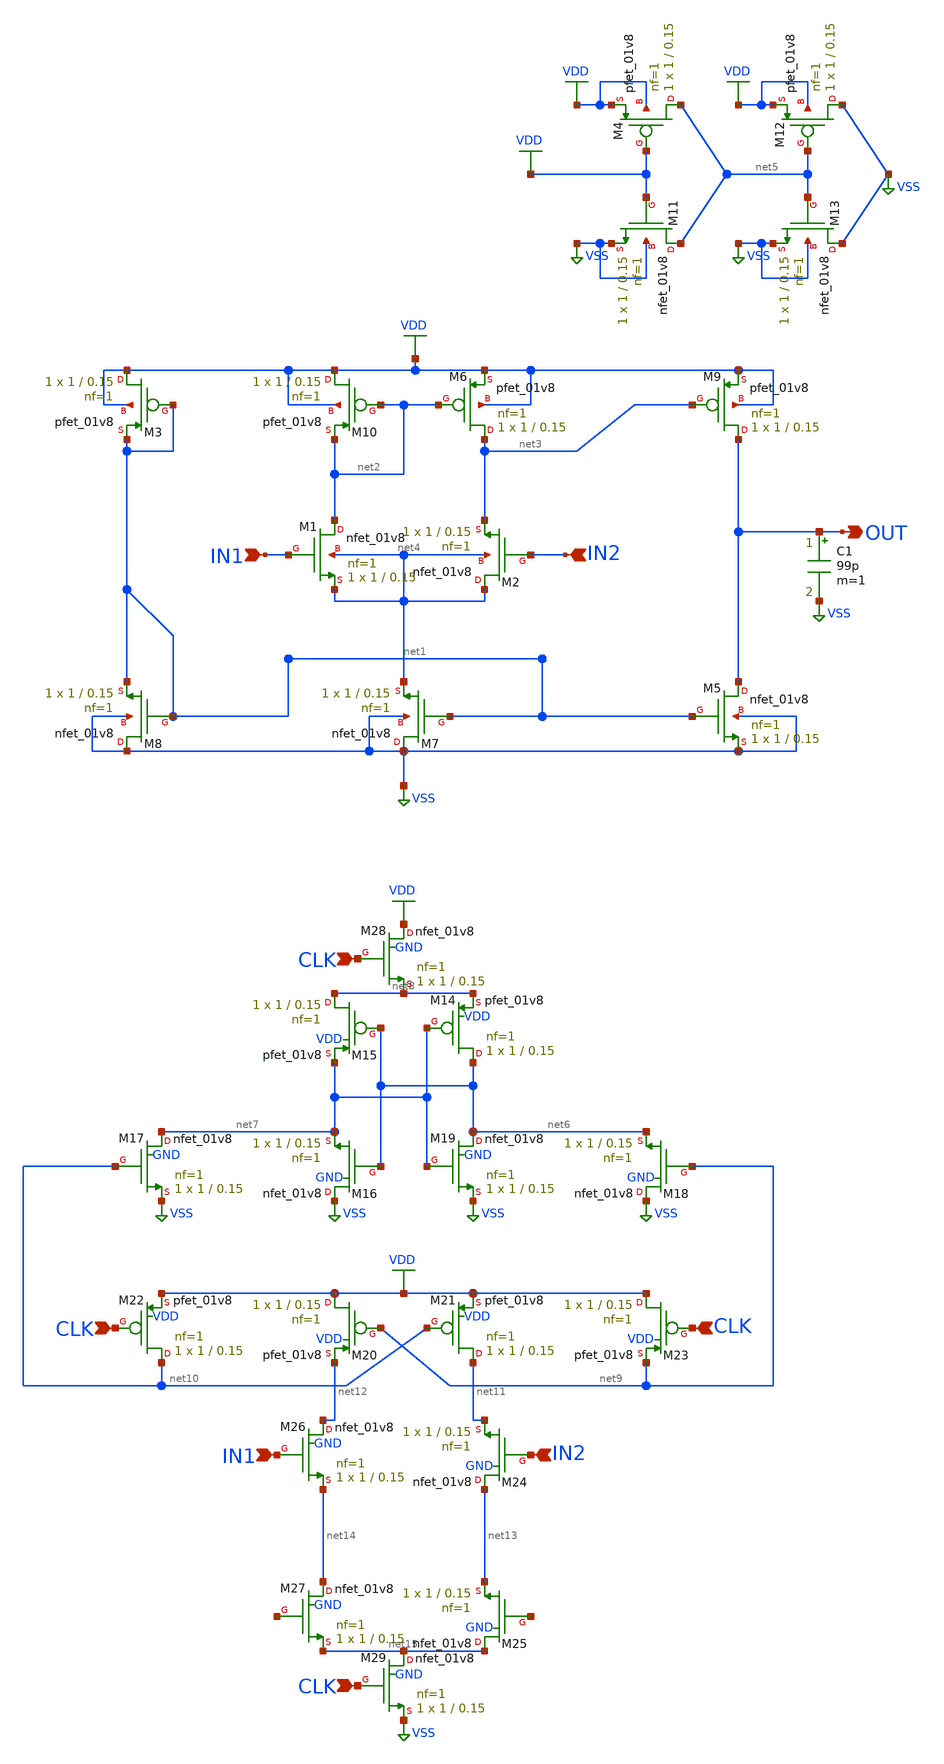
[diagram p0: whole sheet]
** sch_path: 1bit_adc/attempt2.sch
**.subckt attempt2 IN1 IN2 OUT CLK CLK CLK IN1 IN2 CLK
*.ipin IN1
*.ipin IN2
*.opin OUT
*.ipin CLK
*.ipin CLK
*.ipin CLK
*.ipin IN1
*.ipin IN2
*.ipin CLK
XM9 OUT net3 VDD VDD sky130_fd_pr__pfet_01v8 L=0.15 W=1 nf=1 ad='int((nf+1)/2) * W/nf * 0.29' as='int((nf+2)/2) * W/nf * 0.29'
+ pd='2*int((nf+1)/2) * (W/nf + 0.29)' ps='2*int((nf+2)/2) * (W/nf + 0.29)' nrd='0.29 / W' nrs='0.29 / W'
+ sa=0 sb=0 sd=0 mult=1 m=1
XM1 net2 IN1 net4 net4 sky130_fd_pr__nfet_01v8 L=0.15 W=1 nf=1 ad='int((nf+1)/2) * W/nf * 0.29' as='int((nf+2)/2) * W/nf * 0.29'
+ pd='2*int((nf+1)/2) * (W/nf + 0.29)' ps='2*int((nf+2)/2) * (W/nf + 0.29)' nrd='0.29 / W' nrs='0.29 / W'
+ sa=0 sb=0 sd=0 mult=1 m=1
XM2 net4 IN2 net3 net4 sky130_fd_pr__nfet_01v8 L=0.15 W=1 nf=1 ad='int((nf+1)/2) * W/nf * 0.29' as='int((nf+2)/2) * W/nf * 0.29'
+ pd='2*int((nf+1)/2) * (W/nf + 0.29)' ps='2*int((nf+2)/2) * (W/nf + 0.29)' nrd='0.29 / W' nrs='0.29 / W'
+ sa=0 sb=0 sd=0 mult=1 m=1
XM5 OUT net1 VSS VSS sky130_fd_pr__nfet_01v8 L=0.15 W=1 nf=1 ad='int((nf+1)/2) * W/nf * 0.29' as='int((nf+2)/2) * W/nf * 0.29'
+ pd='2*int((nf+1)/2) * (W/nf + 0.29)' ps='2*int((nf+2)/2) * (W/nf + 0.29)' nrd='0.29 / W' nrs='0.29 / W'
+ sa=0 sb=0 sd=0 mult=1 m=1
XM7 VSS net1 net4 VSS sky130_fd_pr__nfet_01v8 L=0.15 W=1 nf=1 ad='int((nf+1)/2) * W/nf * 0.29' as='int((nf+2)/2) * W/nf * 0.29'
+ pd='2*int((nf+1)/2) * (W/nf + 0.29)' ps='2*int((nf+2)/2) * (W/nf + 0.29)' nrd='0.29 / W' nrs='0.29 / W'
+ sa=0 sb=0 sd=0 mult=1 m=1
XM8 VSS net1 net1 VSS sky130_fd_pr__nfet_01v8 L=0.15 W=1 nf=1 ad='int((nf+1)/2) * W/nf * 0.29' as='int((nf+2)/2) * W/nf * 0.29'
+ pd='2*int((nf+1)/2) * (W/nf + 0.29)' ps='2*int((nf+2)/2) * (W/nf + 0.29)' nrd='0.29 / W' nrs='0.29 / W'
+ sa=0 sb=0 sd=0 mult=1 m=1
XM6 net3 net2 VDD VDD sky130_fd_pr__pfet_01v8 L=0.15 W=1 nf=1 ad='int((nf+1)/2) * W/nf * 0.29' as='int((nf+2)/2) * W/nf * 0.29'
+ pd='2*int((nf+1)/2) * (W/nf + 0.29)' ps='2*int((nf+2)/2) * (W/nf + 0.29)' nrd='0.29 / W' nrs='0.29 / W'
+ sa=0 sb=0 sd=0 mult=1 m=1
XM10 VDD net2 net2 VDD sky130_fd_pr__pfet_01v8 L=0.15 W=1 nf=1 ad='int((nf+1)/2) * W/nf * 0.29' as='int((nf+2)/2) * W/nf * 0.29'
+ pd='2*int((nf+1)/2) * (W/nf + 0.29)' ps='2*int((nf+2)/2) * (W/nf + 0.29)' nrd='0.29 / W' nrs='0.29 / W'
+ sa=0 sb=0 sd=0 mult=1 m=1
XM3 VDD net1 net1 VDD sky130_fd_pr__pfet_01v8 L=0.15 W=1 nf=1 ad='int((nf+1)/2) * W/nf * 0.29' as='int((nf+2)/2) * W/nf * 0.29'
+ pd='2*int((nf+1)/2) * (W/nf + 0.29)' ps='2*int((nf+2)/2) * (W/nf + 0.29)' nrd='0.29 / W' nrs='0.29 / W'
+ sa=0 sb=0 sd=0 mult=1 m=1
XM4 net5 VDD VDD VDD sky130_fd_pr__pfet_01v8 L=0.15 W=1 nf=1 ad='int((nf+1)/2) * W/nf * 0.29' as='int((nf+2)/2) * W/nf * 0.29'
+ pd='2*int((nf+1)/2) * (W/nf + 0.29)' ps='2*int((nf+2)/2) * (W/nf + 0.29)' nrd='0.29 / W' nrs='0.29 / W'
+ sa=0 sb=0 sd=0 mult=1 m=1
XM11 net5 VDD VSS VSS sky130_fd_pr__nfet_01v8 L=0.15 W=1 nf=1 ad='int((nf+1)/2) * W/nf * 0.29' as='int((nf+2)/2) * W/nf * 0.29'
+ pd='2*int((nf+1)/2) * (W/nf + 0.29)' ps='2*int((nf+2)/2) * (W/nf + 0.29)' nrd='0.29 / W' nrs='0.29 / W'
+ sa=0 sb=0 sd=0 mult=1 m=1
XM12 VSS net5 VDD VDD sky130_fd_pr__pfet_01v8 L=0.15 W=1 nf=1 ad='int((nf+1)/2) * W/nf * 0.29' as='int((nf+2)/2) * W/nf * 0.29'
+ pd='2*int((nf+1)/2) * (W/nf + 0.29)' ps='2*int((nf+2)/2) * (W/nf + 0.29)' nrd='0.29 / W' nrs='0.29 / W'
+ sa=0 sb=0 sd=0 mult=1 m=1
XM13 VSS net5 VSS VSS sky130_fd_pr__nfet_01v8 L=0.15 W=1 nf=1 ad='int((nf+1)/2) * W/nf * 0.29' as='int((nf+2)/2) * W/nf * 0.29'
+ pd='2*int((nf+1)/2) * (W/nf + 0.29)' ps='2*int((nf+2)/2) * (W/nf + 0.29)' nrd='0.29 / W' nrs='0.29 / W'
+ sa=0 sb=0 sd=0 mult=1 m=1
C1 OUT VSS 99p m=1
XM16 VSS net6 net7 GND sky130_fd_pr__nfet_01v8 L=0.15 W=1 nf=1 ad='int((nf+1)/2) * W/nf * 0.29' as='int((nf+2)/2) * W/nf * 0.29'
+ pd='2*int((nf+1)/2) * (W/nf + 0.29)' ps='2*int((nf+2)/2) * (W/nf + 0.29)' nrd='0.29 / W' nrs='0.29 / W'
+ sa=0 sb=0 sd=0 mult=1 m=1
XM17 net7 net10 VSS GND sky130_fd_pr__nfet_01v8 L=0.15 W=1 nf=1 ad='int((nf+1)/2) * W/nf * 0.29' as='int((nf+2)/2) * W/nf * 0.29'
+ pd='2*int((nf+1)/2) * (W/nf + 0.29)' ps='2*int((nf+2)/2) * (W/nf + 0.29)' nrd='0.29 / W' nrs='0.29 / W'
+ sa=0 sb=0 sd=0 mult=1 m=1
XM18 VSS net9 net6 GND sky130_fd_pr__nfet_01v8 L=0.15 W=1 nf=1 ad='int((nf+1)/2) * W/nf * 0.29' as='int((nf+2)/2) * W/nf * 0.29'
+ pd='2*int((nf+1)/2) * (W/nf + 0.29)' ps='2*int((nf+2)/2) * (W/nf + 0.29)' nrd='0.29 / W' nrs='0.29 / W'
+ sa=0 sb=0 sd=0 mult=1 m=1
XM19 net6 net7 VSS GND sky130_fd_pr__nfet_01v8 L=0.15 W=1 nf=1 ad='int((nf+1)/2) * W/nf * 0.29' as='int((nf+2)/2) * W/nf * 0.29'
+ pd='2*int((nf+1)/2) * (W/nf + 0.29)' ps='2*int((nf+2)/2) * (W/nf + 0.29)' nrd='0.29 / W' nrs='0.29 / W'
+ sa=0 sb=0 sd=0 mult=1 m=1
XM24 net13 IN2 net11 GND sky130_fd_pr__nfet_01v8 L=0.15 W=1 nf=1 ad='int((nf+1)/2) * W/nf * 0.29' as='int((nf+2)/2) * W/nf * 0.29'
+ pd='2*int((nf+1)/2) * (W/nf + 0.29)' ps='2*int((nf+2)/2) * (W/nf + 0.29)' nrd='0.29 / W' nrs='0.29 / W'
+ sa=0 sb=0 sd=0 mult=1 m=1
XM25 net15 net16 net13 GND sky130_fd_pr__nfet_01v8 L=0.15 W=1 nf=1 ad='int((nf+1)/2) * W/nf * 0.29' as='int((nf+2)/2) * W/nf * 0.29'
+ pd='2*int((nf+1)/2) * (W/nf + 0.29)' ps='2*int((nf+2)/2) * (W/nf + 0.29)' nrd='0.29 / W' nrs='0.29 / W'
+ sa=0 sb=0 sd=0 mult=1 m=1
XM26 net12 IN1 net14 GND sky130_fd_pr__nfet_01v8 L=0.15 W=1 nf=1 ad='int((nf+1)/2) * W/nf * 0.29' as='int((nf+2)/2) * W/nf * 0.29'
+ pd='2*int((nf+1)/2) * (W/nf + 0.29)' ps='2*int((nf+2)/2) * (W/nf + 0.29)' nrd='0.29 / W' nrs='0.29 / W'
+ sa=0 sb=0 sd=0 mult=1 m=1
XM27 net14 net17 net15 GND sky130_fd_pr__nfet_01v8 L=0.15 W=1 nf=1 ad='int((nf+1)/2) * W/nf * 0.29' as='int((nf+2)/2) * W/nf * 0.29'
+ pd='2*int((nf+1)/2) * (W/nf + 0.29)' ps='2*int((nf+2)/2) * (W/nf + 0.29)' nrd='0.29 / W' nrs='0.29 / W'
+ sa=0 sb=0 sd=0 mult=1 m=1
XM28 VDD CLK net8 GND sky130_fd_pr__nfet_01v8 L=0.15 W=1 nf=1 ad='int((nf+1)/2) * W/nf * 0.29' as='int((nf+2)/2) * W/nf * 0.29'
+ pd='2*int((nf+1)/2) * (W/nf + 0.29)' ps='2*int((nf+2)/2) * (W/nf + 0.29)' nrd='0.29 / W' nrs='0.29 / W'
+ sa=0 sb=0 sd=0 mult=1 m=1
XM23 VDD CLK net9 VDD sky130_fd_pr__pfet_01v8 L=0.15 W=1 nf=1 ad='int((nf+1)/2) * W/nf * 0.29' as='int((nf+2)/2) * W/nf * 0.29'
+ pd='2*int((nf+1)/2) * (W/nf + 0.29)' ps='2*int((nf+2)/2) * (W/nf + 0.29)' nrd='0.29 / W' nrs='0.29 / W'
+ sa=0 sb=0 sd=0 mult=1 m=1
XM21 net11 net10 VDD VDD sky130_fd_pr__pfet_01v8 L=0.15 W=1 nf=1 ad='int((nf+1)/2) * W/nf * 0.29' as='int((nf+2)/2) * W/nf * 0.29'
+ pd='2*int((nf+1)/2) * (W/nf + 0.29)' ps='2*int((nf+2)/2) * (W/nf + 0.29)' nrd='0.29 / W' nrs='0.29 / W'
+ sa=0 sb=0 sd=0 mult=1 m=1
XM20 VDD net9 net12 VDD sky130_fd_pr__pfet_01v8 L=0.15 W=1 nf=1 ad='int((nf+1)/2) * W/nf * 0.29' as='int((nf+2)/2) * W/nf * 0.29'
+ pd='2*int((nf+1)/2) * (W/nf + 0.29)' ps='2*int((nf+2)/2) * (W/nf + 0.29)' nrd='0.29 / W' nrs='0.29 / W'
+ sa=0 sb=0 sd=0 mult=1 m=1
XM22 net10 CLK VDD VDD sky130_fd_pr__pfet_01v8 L=0.15 W=1 nf=1 ad='int((nf+1)/2) * W/nf * 0.29' as='int((nf+2)/2) * W/nf * 0.29'
+ pd='2*int((nf+1)/2) * (W/nf + 0.29)' ps='2*int((nf+2)/2) * (W/nf + 0.29)' nrd='0.29 / W' nrs='0.29 / W'
+ sa=0 sb=0 sd=0 mult=1 m=1
XM14 net6 net7 net8 VDD sky130_fd_pr__pfet_01v8 L=0.15 W=1 nf=1 ad='int((nf+1)/2) * W/nf * 0.29' as='int((nf+2)/2) * W/nf * 0.29'
+ pd='2*int((nf+1)/2) * (W/nf + 0.29)' ps='2*int((nf+2)/2) * (W/nf + 0.29)' nrd='0.29 / W' nrs='0.29 / W'
+ sa=0 sb=0 sd=0 mult=1 m=1
XM15 net8 net6 net7 VDD sky130_fd_pr__pfet_01v8 L=0.15 W=1 nf=1 ad='int((nf+1)/2) * W/nf * 0.29' as='int((nf+2)/2) * W/nf * 0.29'
+ pd='2*int((nf+1)/2) * (W/nf + 0.29)' ps='2*int((nf+2)/2) * (W/nf + 0.29)' nrd='0.29 / W' nrs='0.29 / W'
+ sa=0 sb=0 sd=0 mult=1 m=1
XM29 net15 CLK VSS GND sky130_fd_pr__nfet_01v8 L=0.15 W=1 nf=1 ad='int((nf+1)/2) * W/nf * 0.29' as='int((nf+2)/2) * W/nf * 0.29'
+ pd='2*int((nf+1)/2) * (W/nf + 0.29)' ps='2*int((nf+2)/2) * (W/nf + 0.29)' nrd='0.29 / W' nrs='0.29 / W'
+ sa=0 sb=0 sd=0 mult=1 m=1
**** begin user architecture code



.options gmin=1e-12

VVDD VDD 0 DC 5
VIN1 IN1 0 SIN(2 1 100k)
VIN2 IN2 0 SIN(2 1 10k)
VGND VSS 0 DC 0


.control
tran 5n 40000n
*plot IN1 IN2
write 1bit_adc.raw all
.endc

.end



** opencircuitdesign pdks install
.lib $::SKYWATER_MODELS/sky130.lib.spice tt
*.lib $::SKYWATER_STDCELLS/sky130_fd_sc_hd.spice tt

**** end user architecture code
**.ends
.GLOBAL VSS
.GLOBAL VDD
.end
